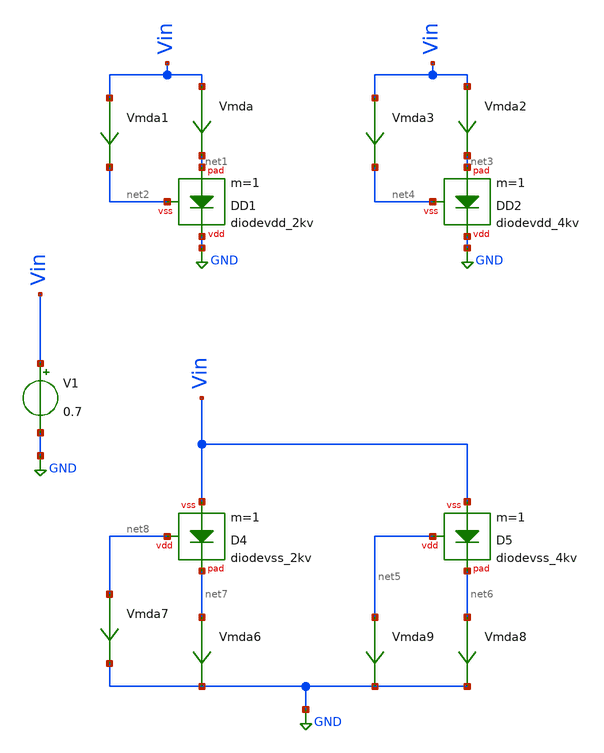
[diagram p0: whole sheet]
** sch_path: ihp-sg13g2/xschem_libs/sg13g2_tests_ase/dc_esd_diodes/schematic/dc_esd_diodes.sch
**.subckt dc_esd_diodes
V1 Vin GND 0.7
Vmda Vin net1 0
.save i(vmda)
Vmda1 Vin net2 0
.save i(vmda1)
XD1 GND net1 net2 diodevdd_2kv m=1
Vmda2 Vin net3 0
.save i(vmda2)
Vmda3 Vin net4 0
.save i(vmda3)
XD2 GND net3 net4 diodevdd_4kv m=1
Vmda6 net7 GND 0
.save i(vmda6)
Vmda7 net8 GND 0
.save i(vmda7)
XD4 net8 net7 Vin diodevss_2kv m=1
Vmda8 net6 GND 0
.save i(vmda8)
Vmda9 net5 GND 0
.save i(vmda9)
XD5 net5 net6 Vin diodevss_4kv m=1
**.ends
.GLOBAL GND
.end
